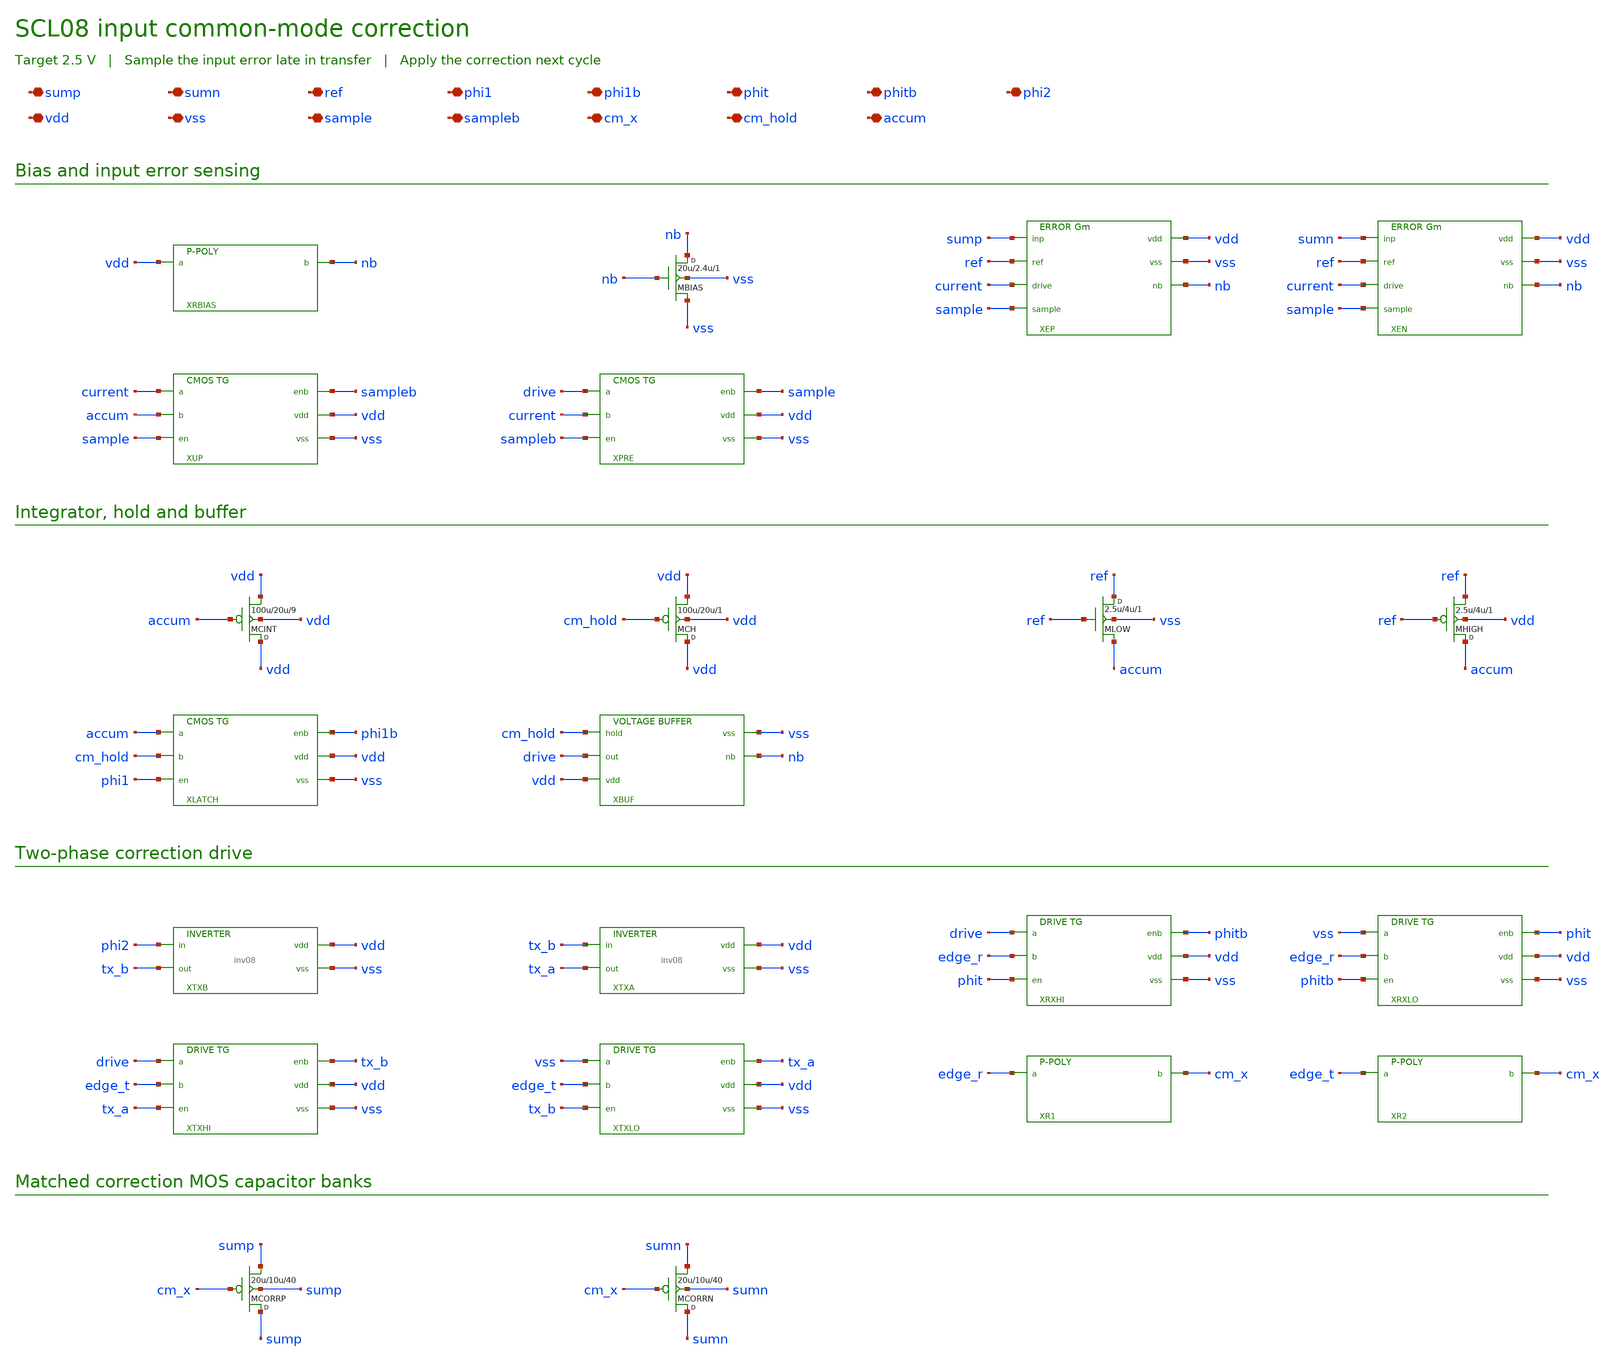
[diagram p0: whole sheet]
** sch_path: ICMC/schematic/icm_cell08.sch
**.subckt icm_cell08 sump sumn ref phi1 phi1b phit phitb phi2 vdd vss sample sampleb cm_x cm_hold
*+ accum
*.iopin sump
*.iopin sumn
*.iopin ref
*.iopin phi1
*.iopin phi1b
*.iopin phit
*.iopin phitb
*.iopin phi2
*.iopin vdd
*.iopin vss
*.iopin sample
*.iopin sampleb
*.iopin cm_x
*.iopin cm_hold
*.iopin accum
XRBIAS vdd nb RPP W=2.4u L=20000u
MBIAS nb nb vss vss N w=20u l=2.4u m=1
XEP sump ref current sample vdd vss nb icm_error08
XEN sumn ref current sample vdd vss nb icm_error08
XUP current accum sample sampleb vdd vss icm_tg08
XPRE drive current sampleb sample vdd vss icm_tg08
MCINT vdd accum vdd vdd P w=100u l=20u m=9
MCH vdd cm_hold vdd vdd P w=100u l=20u m=1
MLOW ref ref accum vss N w=2.5u l=4u m=1
MHIGH accum ref ref vdd P w=2.5u l=4u m=1
XLATCH accum cm_hold phi1 phi1b vdd vss icm_tg08
XBUF cm_hold drive vdd vss nb icm_buffer08
XTXB phi2 tx_b vdd vss inv08 w=3u
XTXA tx_b tx_a vdd vss inv08 w=12u
XRXHI drive edge_r phit phitb vdd vss icm_drive_tg08
XRXLO vss edge_r phitb phit vdd vss icm_drive_tg08
XTXHI drive edge_t tx_a tx_b vdd vss icm_drive_tg08
XTXLO vss edge_t tx_b tx_a vdd vss icm_drive_tg08
XR1 edge_r cm_x RPP W=2.4u L=350u
XR2 edge_t cm_x RPP W=2.4u L=744u
MCORRP sump cm_x sump sump P w=20u l=10u ad=90p as=90p pd=49u ps=49u m=40
MCORRN sumn cm_x sumn sumn P w=20u l=10u ad=90p as=90p pd=49u ps=49u m=40
**.ends

* expanding   symbol:  icm_error08.sym # of pins=7
** sym_path: ICMC/schematic/icm_error08.sym
** sch_path: ICMC/schematic/icm_error08.sch
.subckt icm_error08 inp ref drive sample vdd vss nb
*.iopin inp
*.iopin ref
*.iopin drive
*.iopin sample
*.iopin vdd
*.iopin vss
*.iopin nb
MREF mirror ref tail vss N w=12u l=2.4u m=1
MSIG drive inp tail vss N w=12u l=2.4u m=1
MEN tail sample sink vss N w=8u l=.8u m=1
MT sink nb vss vss N w=6u l=8u m=1
MP0 mirror mirror vdd vdd P w=12u l=4u m=1
MP1 drive mirror vdd vdd P w=12u l=4u m=1
.ends


* expanding   symbol:  icm_tg08.sym # of pins=6
** sym_path: ICMC/schematic/icm_tg08.sym
** sch_path: ICMC/schematic/icm_tg08.sch
.subckt icm_tg08 a b en enb vdd vss
*.iopin a
*.iopin b
*.iopin en
*.iopin enb
*.iopin vdd
*.iopin vss
MN a en b vss N w=4u l=.8u ad=18p as=18p pd=17u ps=17u m=1
MP a enb b vdd P w=8u l=.8u ad=36p as=36p pd=25u ps=25u m=1
.ends


* expanding   symbol:  icm_buffer08.sym # of pins=5
** sym_path: ICMC/schematic/icm_buffer08.sym
** sch_path: ICMC/schematic/icm_buffer08.sch
.subckt icm_buffer08 hold out vdd vss nb
*.iopin hold
*.iopin out
*.iopin vdd
*.iopin vss
*.iopin nb
MIN nleft out tail vss N w=20u l=2.4u m=1
MREF gain hold tail vss N w=20u l=2.4u m=1
MTAIL tail nb vss vss N w=8u l=4.8u m=1
MP0 nleft nleft vdd vdd P w=10u l=3.2u m=1
MP1 gain nleft vdd vdd P w=10u l=3.2u m=1
MP2 out gain vdd vdd P w=100u l=1.6u m=1
MN2 out nb vss vss N w=12u l=4.8u m=1
MCOMP out gain out out P w=30u l=12u m=2
.ends


* expanding   symbol:  icm_drive_tg08.sym # of pins=6
** sym_path: ICMC/schematic/icm_drive_tg08.sym
** sch_path: ICMC/schematic/icm_drive_tg08.sch
.subckt icm_drive_tg08 a b en enb vdd vss
*.iopin a
*.iopin b
*.iopin en
*.iopin enb
*.iopin vdd
*.iopin vss
MN a en b vss N w=12u l=.8u ad=54p as=54p pd=33u ps=33u m=1
MP a enb b vdd P w=24u l=.8u ad=108p as=108p pd=57u ps=57u m=1
.ends

.end
